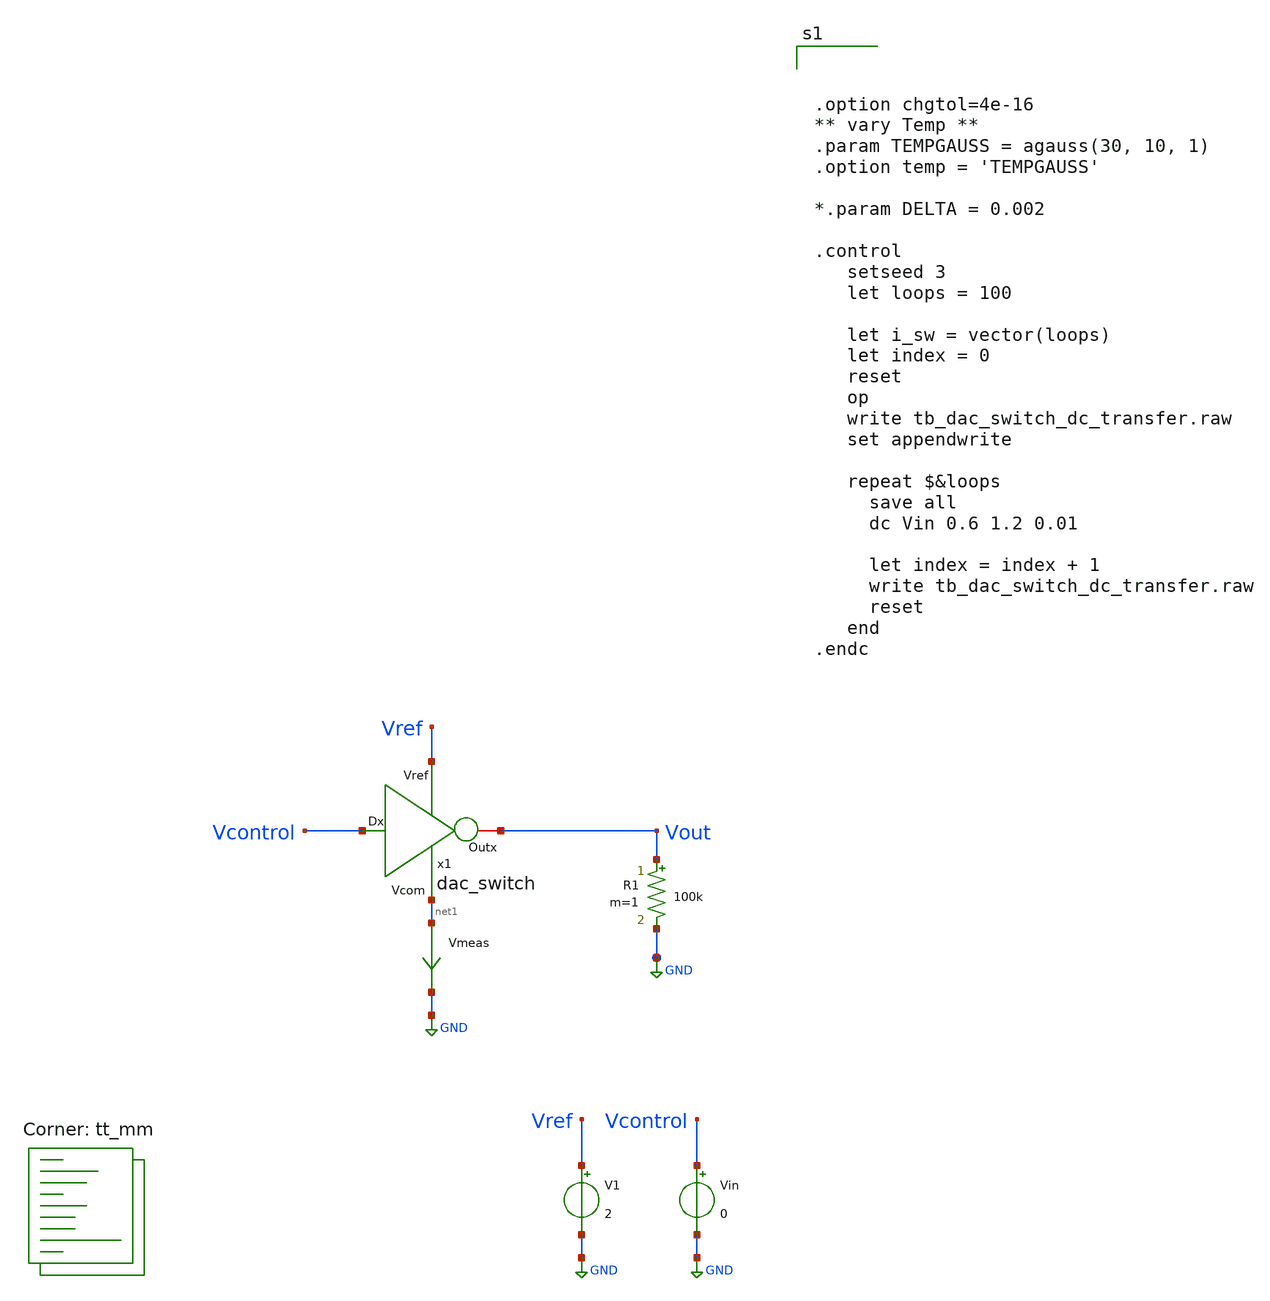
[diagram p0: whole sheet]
** sch_path: xschem/tb_dac_switch_dc_transfer.sch
**.subckt tb_dac_switch_dc_transfer
V1 Vref GND 2
x1 Vref Vcontrol Vout net1 dac_switch
Vin Vcontrol GND 0
Vmeas net1 GND 0
.save i(vmeas)
R1 Vout GND 100k m=1
**** begin user architecture code
.lib $::SKYWATER_MODELS/sky130.lib.spice tt_mm



.option chgtol=4e-16
** vary Temp **
.param TEMPGAUSS = agauss(30, 10, 1)
.option temp = 'TEMPGAUSS'

*.param DELTA = 0.002

.control
   setseed 3
   let loops = 100

   let i_sw = vector(loops)
   let index = 0
   reset
   op
   write tb_dac_switch_dc_transfer.raw
   set appendwrite

   repeat $&loops
     save all
     dc Vin 0.6 1.2 0.01

     let index = index + 1
     write tb_dac_switch_dc_transfer.raw
     reset
   end
.endc



**** end user architecture code
**.ends

* expanding   symbol:  dac_switch.sym # of pins=4
** sym_path: xschem/dac_switch.sym
** sch_path: xschem/dac_switch.sch
.subckt dac_switch Vref Dx Outx Vcom
*.ipin Dx
*.opin Outx
*.iopin Vref
*.iopin Vcom
XM1 Outx Dx Vref Vref sky130_fd_pr__pfet_g5v0d10v5 L=0.5 W=16 nf=1 ad='int((nf+1)/2) * W/nf * 0.29' as='int((nf+2)/2) * W/nf * 0.29'
+ pd='2*int((nf+1)/2) * (W/nf + 0.29)' ps='2*int((nf+2)/2) * (W/nf + 0.29)' nrd='0.29 / W' nrs='0.29 / W'
+ sa=0 sb=0 sd=0 mult=1 m=1
XM2 Outx Dx Vcom Vcom sky130_fd_pr__nfet_g5v0d10v5 L=0.5 W=7 nf=1 ad='int((nf+1)/2) * W/nf * 0.29' as='int((nf+2)/2) * W/nf * 0.29'
+ pd='2*int((nf+1)/2) * (W/nf + 0.29)' ps='2*int((nf+2)/2) * (W/nf + 0.29)' nrd='0.29 / W' nrs='0.29 / W'
+ sa=0 sb=0 sd=0 mult=1 m=1
.ends

.GLOBAL GND
.end
